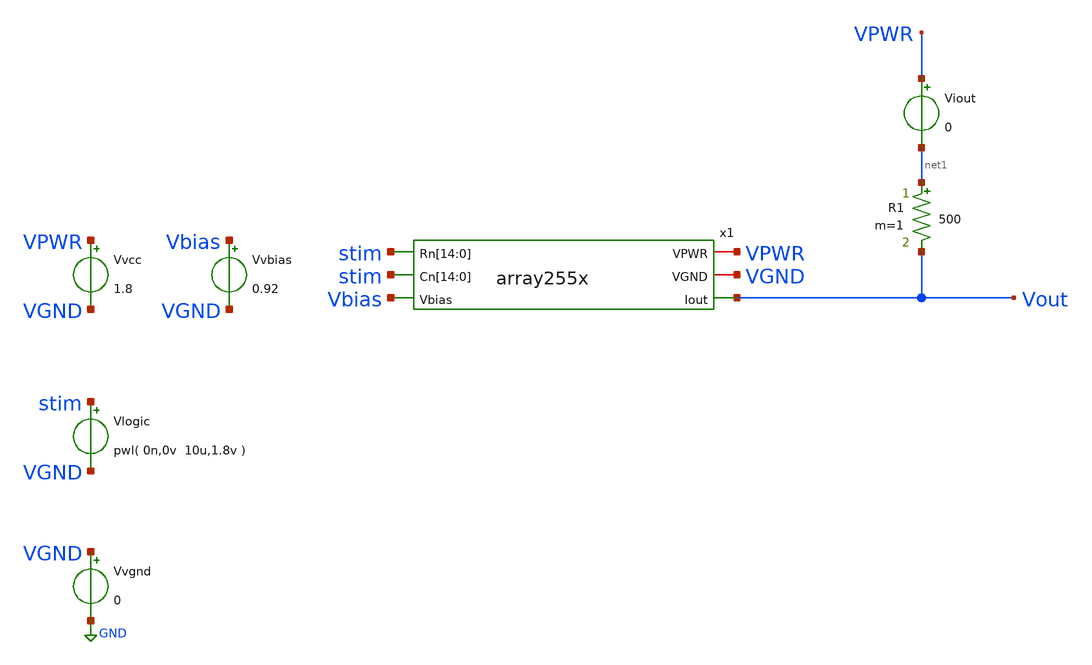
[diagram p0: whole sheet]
** sch_path: xschem/tb_array255x.sch
**.subckt tb_array255x
Vvcc VPWR VGND 1.8
R1 net1 Vout 500 m=1
Vvbias Vbias VGND 0.92
Vvgnd VGND GND 0
Viout VPWR net1 0
Vlogic stim VGND pwl( 0n,0v 10u,1.8v )
x1 VPWR VGND stim stim stim stim stim stim stim stim stim stim stim stim stim stim stim stim stim
+ stim stim stim stim stim stim stim stim stim stim stim stim stim Vbias Vout array255x
**** begin user architecture code



*.options savecurrents
.control

    save all
    tran 1n 12.8u
    write tb_array255x.raw vout

.endc




.lib $::SKYWATER_MODELS/sky130.lib.spice tt
.include $::SKYWATER_STDCELLS/sky130_fd_sc_hd.spice

**** end user architecture code
**.ends

* expanding   symbol:  array255x.sym # of pins=6
** sym_path: xschem/array255x.sym
** sch_path: xschem/array255x.sch
.subckt array255x VPWR VGND Rn[14] Rn[13] Rn[12] Rn[11] Rn[10] Rn[9] Rn[8] Rn[7] Rn[6] Rn[5] Rn[4]
+ Rn[3] Rn[2] Rn[1] Rn[0] Cn[14] Cn[13] Cn[12] Cn[11] Cn[10] Cn[9] Cn[8] Cn[7] Cn[6] Cn[5] Cn[4] Cn[3]
+ Cn[2] Cn[1] Cn[0] Vbias Iout
*.iopin VPWR
*.opin Iout
*.iopin VGND
*.ipin Vbias
*.ipin
*+ Cn[14],Cn[13],Cn[12],Cn[11],Cn[10],Cn[9],Cn[8],Cn[7],Cn[6],Cn[5],Cn[4],Cn[3],Cn[2],Cn[1],Cn[0]
*.ipin
*+ Rn[14],Rn[13],Rn[12],Rn[11],Rn[10],Rn[9],Rn[8],Rn[7],Rn[6],Rn[5],Rn[4],Rn[3],Rn[2],Rn[1],Rn[0]
XIR[14] Vbias VPWR Rn[14] Rn[13] Cn[14] Cn[13] Cn[12] Cn[11] Cn[10] Cn[9] Cn[8] Cn[7] Cn[6] Cn[5]
+ Cn[4] Cn[3] Cn[2] Cn[1] Cn[0] VGND Iout row15x
XIR[13] Vbias VPWR Rn[13] Rn[12] Cn[14] Cn[13] Cn[12] Cn[11] Cn[10] Cn[9] Cn[8] Cn[7] Cn[6] Cn[5]
+ Cn[4] Cn[3] Cn[2] Cn[1] Cn[0] VGND Iout row15x
XIR[12] Vbias VPWR Rn[12] Rn[11] Cn[14] Cn[13] Cn[12] Cn[11] Cn[10] Cn[9] Cn[8] Cn[7] Cn[6] Cn[5]
+ Cn[4] Cn[3] Cn[2] Cn[1] Cn[0] VGND Iout row15x
XIR[11] Vbias VPWR Rn[11] Rn[10] Cn[14] Cn[13] Cn[12] Cn[11] Cn[10] Cn[9] Cn[8] Cn[7] Cn[6] Cn[5]
+ Cn[4] Cn[3] Cn[2] Cn[1] Cn[0] VGND Iout row15x
XIR[10] Vbias VPWR Rn[10] Rn[9] Cn[14] Cn[13] Cn[12] Cn[11] Cn[10] Cn[9] Cn[8] Cn[7] Cn[6] Cn[5]
+ Cn[4] Cn[3] Cn[2] Cn[1] Cn[0] VGND Iout row15x
XIR[9] Vbias VPWR Rn[9] Rn[8] Cn[14] Cn[13] Cn[12] Cn[11] Cn[10] Cn[9] Cn[8] Cn[7] Cn[6] Cn[5] Cn[4]
+ Cn[3] Cn[2] Cn[1] Cn[0] VGND Iout row15x
XIR[8] Vbias VPWR Rn[8] Rn[7] Cn[14] Cn[13] Cn[12] Cn[11] Cn[10] Cn[9] Cn[8] Cn[7] Cn[6] Cn[5] Cn[4]
+ Cn[3] Cn[2] Cn[1] Cn[0] VGND Iout row15x
XIR[7] Vbias VPWR Rn[7] Rn[6] Cn[14] Cn[13] Cn[12] Cn[11] Cn[10] Cn[9] Cn[8] Cn[7] Cn[6] Cn[5] Cn[4]
+ Cn[3] Cn[2] Cn[1] Cn[0] VGND Iout row15x
XIR[6] Vbias VPWR Rn[6] Rn[5] Cn[14] Cn[13] Cn[12] Cn[11] Cn[10] Cn[9] Cn[8] Cn[7] Cn[6] Cn[5] Cn[4]
+ Cn[3] Cn[2] Cn[1] Cn[0] VGND Iout row15x
XIR[5] Vbias VPWR Rn[5] Rn[4] Cn[14] Cn[13] Cn[12] Cn[11] Cn[10] Cn[9] Cn[8] Cn[7] Cn[6] Cn[5] Cn[4]
+ Cn[3] Cn[2] Cn[1] Cn[0] VGND Iout row15x
XIR[4] Vbias VPWR Rn[4] Rn[3] Cn[14] Cn[13] Cn[12] Cn[11] Cn[10] Cn[9] Cn[8] Cn[7] Cn[6] Cn[5] Cn[4]
+ Cn[3] Cn[2] Cn[1] Cn[0] VGND Iout row15x
XIR[3] Vbias VPWR Rn[3] Rn[2] Cn[14] Cn[13] Cn[12] Cn[11] Cn[10] Cn[9] Cn[8] Cn[7] Cn[6] Cn[5] Cn[4]
+ Cn[3] Cn[2] Cn[1] Cn[0] VGND Iout row15x
XIR[2] Vbias VPWR Rn[2] Rn[1] Cn[14] Cn[13] Cn[12] Cn[11] Cn[10] Cn[9] Cn[8] Cn[7] Cn[6] Cn[5] Cn[4]
+ Cn[3] Cn[2] Cn[1] Cn[0] VGND Iout row15x
XIR[1] Vbias VPWR Rn[1] Rn[0] Cn[14] Cn[13] Cn[12] Cn[11] Cn[10] Cn[9] Cn[8] Cn[7] Cn[6] Cn[5] Cn[4]
+ Cn[3] Cn[2] Cn[1] Cn[0] VGND Iout row15x
XIR[0] Vbias VPWR Rn[0] VGND Cn[14] Cn[13] Cn[12] Cn[11] Cn[10] Cn[9] Cn[8] Cn[7] Cn[6] Cn[5] Cn[4]
+ Cn[3] Cn[2] Cn[1] Cn[0] VGND Iout row15x
XIR[15] Vbias VPWR VPWR Rn[14] Cn[14] Cn[13] Cn[12] Cn[11] Cn[10] Cn[9] Cn[8] Cn[7] Cn[6] Cn[5]
+ Cn[4] Cn[3] Cn[2] Cn[1] Cn[0] VGND Iout row15x
.ends


* expanding   symbol:  row15x.sym # of pins=7
** sym_path: xschem/row15x.sym
** sch_path: xschem/row15x.sch
.subckt row15x Vbias VPWR Sn Rn Cn[14] Cn[13] Cn[12] Cn[11] Cn[10] Cn[9] Cn[8] Cn[7] Cn[6] Cn[5]
+ Cn[4] Cn[3] Cn[2] Cn[1] Cn[0] VGND Iout
*.ipin Sn
*.ipin Rn
*.ipin
*+ Cn[14],Cn[13],Cn[12],Cn[11],Cn[10],Cn[9],Cn[8],Cn[7],Cn[6],Cn[5],Cn[4],Cn[3],Cn[2],Cn[1],Cn[0]
*.iopin VPWR
*.iopin VGND
*.opin Iout
*.ipin Vbias
XIC[14] VPWR VGND Rn Cn[14] Sn Vbias Iout icell
XIC[13] VPWR VGND Rn Cn[13] Sn Vbias Iout icell
XIC[12] VPWR VGND Rn Cn[12] Sn Vbias Iout icell
XIC[11] VPWR VGND Rn Cn[11] Sn Vbias Iout icell
XIC[10] VPWR VGND Rn Cn[10] Sn Vbias Iout icell
XIC[9] VPWR VGND Rn Cn[9] Sn Vbias Iout icell
XIC[8] VPWR VGND Rn Cn[8] Sn Vbias Iout icell
XIC[7] VPWR VGND Rn Cn[7] Sn Vbias Iout icell
XIC[6] VPWR VGND Rn Cn[6] Sn Vbias Iout icell
XIC[5] VPWR VGND Rn Cn[5] Sn Vbias Iout icell
XIC[4] VPWR VGND Rn Cn[4] Sn Vbias Iout icell
XIC[3] VPWR VGND Rn Cn[3] Sn Vbias Iout icell
XIC[2] VPWR VGND Rn Cn[2] Sn Vbias Iout icell
XIC[1] VPWR VGND Rn Cn[1] Sn Vbias Iout icell
XIC[0] VPWR VGND Rn Cn[0] Sn Vbias Iout icell
XIC[15] VPWR VGND VPWR VPWR Sn Vbias Iout icell
XIC_dummy_left VPWR VGND VPWR VPWR VPWR VGND net1 icell
XIC_dummy_right VPWR VGND VPWR VPWR VPWR VGND net2 icell
.ends


* expanding   symbol:  icell.sym # of pins=7
** sym_path: xschem/icell.sym
** sch_path: xschem/icell.sch
.subckt icell VPWR VGND Rn Cn Sn Vbias Iout
*.ipin Rn
*.iopin VPWR
*.opin Iout
*.iopin VGND
*.ipin Cn
*.ipin Sn
*.ipin Vbias
XMsp Ien Sn VPWR VPWR sky130_fd_pr__pfet_01v8 L=0.15 W=0.5 nf=1 ad='int((nf+1)/2) * W/nf * 0.29' as='int((nf+2)/2) * W/nf * 0.29'
+ pd='2*int((nf+1)/2) * (W/nf + 0.29)' ps='2*int((nf+2)/2) * (W/nf + 0.29)' nrd='0.29 / W' nrs='0.29 / W'
+ sa=0 sb=0 sd=0 mult=1 m=1
XMsna Ien Sn PDM VGND sky130_fd_pr__nfet_01v8 L=0.15 W=0.5 nf=1 ad='int((nf+1)/2) * W/nf * 0.29' as='int((nf+2)/2) * W/nf * 0.29'
+ pd='2*int((nf+1)/2) * (W/nf + 0.29)' ps='2*int((nf+2)/2) * (W/nf + 0.29)' nrd='0.29 / W' nrs='0.29 / W'
+ sa=0 sb=0 sd=0 mult=1 m=1
XMcpa Ien Cn PUM VPWR sky130_fd_pr__pfet_01v8 L=0.15 W=0.5 nf=1 ad='int((nf+1)/2) * W/nf * 0.29' as='int((nf+2)/2) * W/nf * 0.29'
+ pd='2*int((nf+1)/2) * (W/nf + 0.29)' ps='2*int((nf+2)/2) * (W/nf + 0.29)' nrd='0.29 / W' nrs='0.29 / W'
+ sa=0 sb=0 sd=0 mult=1 m=1
XMrpa PUM Rn VPWR VPWR sky130_fd_pr__pfet_01v8 L=0.15 W=0.5 nf=1 ad='int((nf+1)/2) * W/nf * 0.29' as='int((nf+2)/2) * W/nf * 0.29'
+ pd='2*int((nf+1)/2) * (W/nf + 0.29)' ps='2*int((nf+2)/2) * (W/nf + 0.29)' nrd='0.29 / W' nrs='0.29 / W'
+ sa=0 sb=0 sd=0 mult=1 m=1
XMrno PDM Rn VGND VGND sky130_fd_pr__nfet_01v8 L=0.15 W=0.5 nf=1 ad='int((nf+1)/2) * W/nf * 0.29' as='int((nf+2)/2) * W/nf * 0.29'
+ pd='2*int((nf+1)/2) * (W/nf + 0.29)' ps='2*int((nf+2)/2) * (W/nf + 0.29)' nrd='0.29 / W' nrs='0.29 / W'
+ sa=0 sb=0 sd=0 mult=1 m=1
XMcno PDM Cn VGND VGND sky130_fd_pr__nfet_01v8 L=0.15 W=0.5 nf=1 ad='int((nf+1)/2) * W/nf * 0.29' as='int((nf+2)/2) * W/nf * 0.29'
+ pd='2*int((nf+1)/2) * (W/nf + 0.29)' ps='2*int((nf+2)/2) * (W/nf + 0.29)' nrd='0.29 / W' nrs='0.29 / W'
+ sa=0 sb=0 sd=0 mult=1 m=1
XMiu SM Vbias VGND VGND sky130_fd_pr__nfet_g5v0d10v5 L=0.5 W=0.5 nf=1 ad='int((nf+1)/2) * W/nf * 0.29'
+ as='int((nf+2)/2) * W/nf * 0.29' pd='2*int((nf+1)/2) * (W/nf + 0.29)' ps='2*int((nf+2)/2) * (W/nf + 0.29)'
+ nrd='0.29 / W' nrs='0.29 / W' sa=0 sb=0 sd=0 mult=1 m=1
XMsw Iout Ien SM VGND sky130_fd_pr__nfet_g5v0d10v5 L=0.5 W=0.5 nf=1 ad='int((nf+1)/2) * W/nf * 0.29'
+ as='int((nf+2)/2) * W/nf * 0.29' pd='2*int((nf+1)/2) * (W/nf + 0.29)' ps='2*int((nf+2)/2) * (W/nf + 0.29)'
+ nrd='0.29 / W' nrs='0.29 / W' sa=0 sb=0 sd=0 mult=1 m=1
.ends

.GLOBAL GND
.end
